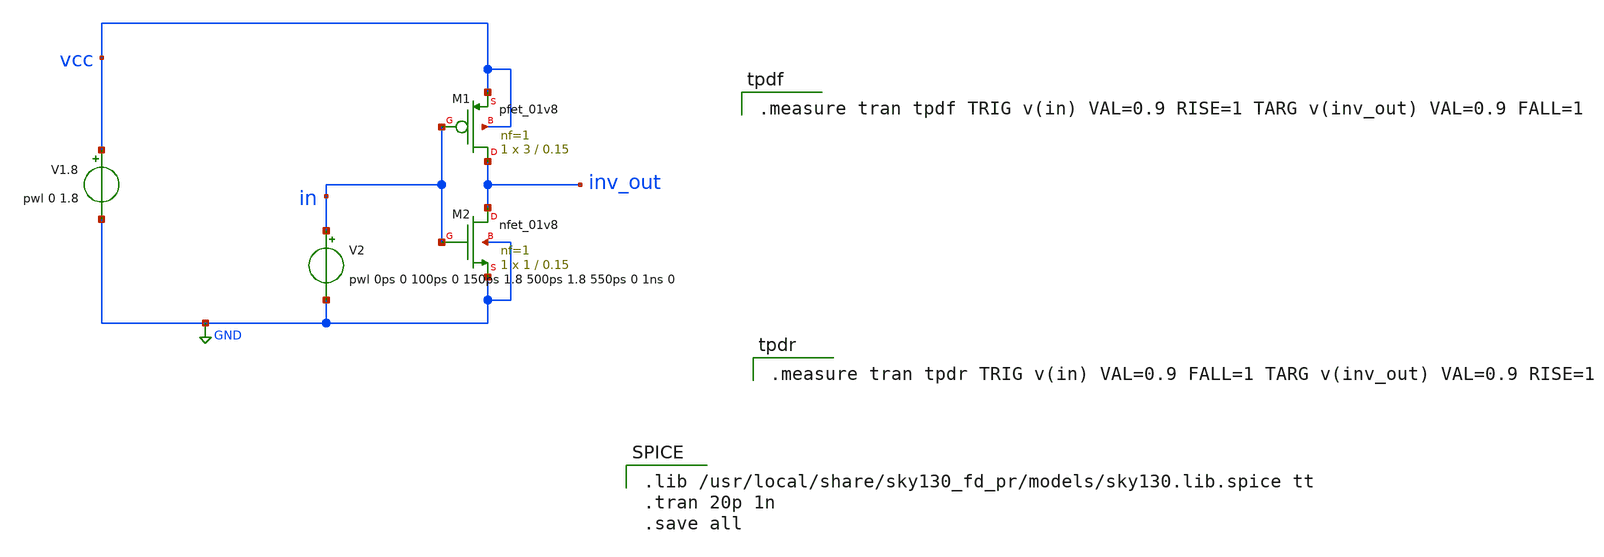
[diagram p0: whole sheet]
** sch_path: projects/inverter/untitled.sch
**.subckt untitled
V1.8 vcc GND pwl 0 1.8
XM2 inv_out in GND GND sky130_fd_pr__nfet_01v8 L=0.15 W=1 nf=1 ad='W * 0.29' as='W * 0.29' pd='W + 2 * 0.29'
+ ps='W + 2 * 0.29' nrd=0 nrs=0 sa=0 sb=0 sd=0 mult=1 m=1
XM1 inv_out in vcc vcc sky130_fd_pr__pfet_01v8 L=0.15 W=3 nf=1 ad='W * 0.29' as='W * 0.29' pd='W + 2 * 0.29'
+ ps='W + 2 * 0.29' nrd=0 nrs=0 sa=0 sb=0 sd=0 mult=1 m=1
V2 in GND pwl 0ps 0 100ps 0 150ps 1.8 500ps 1.8 550ps 0 1ns 0
**** begin user architecture code

.lib /usr/local/share/sky130_fd_pr/models/sky130.lib.spice tt
.tran 20p 1n
.save all


.measure tran tpdr TRIG v(in) VAL=0.9 FALL=1 TARG v(inv_out) VAL=0.9 RISE=1


.measure tran tpdf TRIG v(in) VAL=0.9 RISE=1 TARG v(inv_out) VAL=0.9 FALL=1

**** end user architecture code
**.ends
.GLOBAL GND
.end
